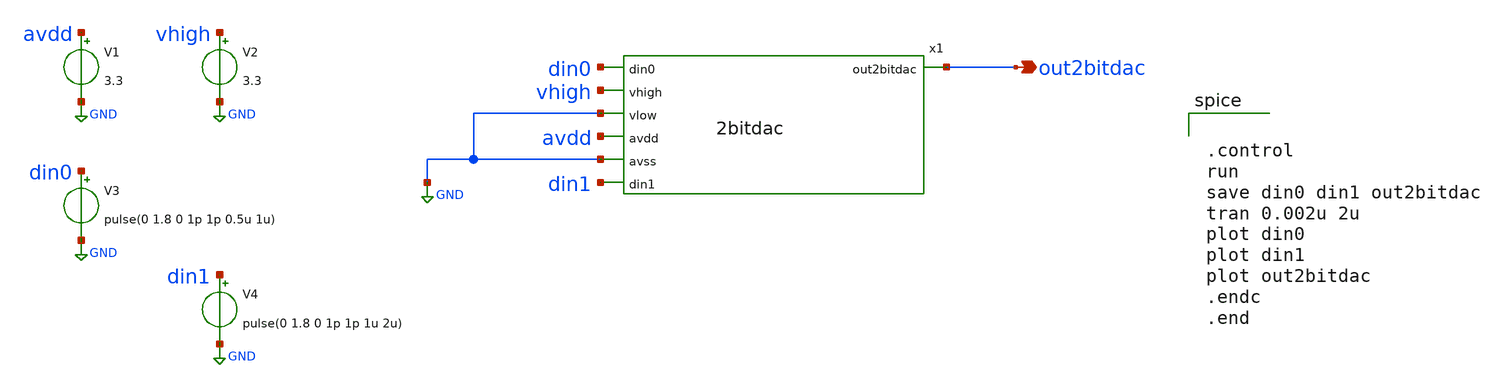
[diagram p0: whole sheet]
** sch_path: xschem/tb_2bitdac.sch
**.subckt tb_2bitdac out2bitdac
*.opin out2bitdac
x1 out2bitdac din0 vhigh GND avdd GND din1 2bitdac
V1 avdd GND 3.3
V2 vhigh GND 3.3
V3 din0 GND pulse(0 1.8 0 1p 1p 0.5u 1u)
V4 din1 GND pulse(0 1.8 0 1p 1p 1u 2u)
**** begin user architecture code

** opencircuitdesign pdks install
.lib $::SKYWATER_MODELS/sky130.lib.spice tt




.control
run
save din0 din1 out2bitdac
tran 0.002u 2u
plot din0
plot din1
plot out2bitdac
.endc
.end

**** end user architecture code
**.ends

* expanding   symbol:  2bitdac.sym # of pins=7
** sym_path: xschem/2bitdac.sym
** sch_path: xschem/2bitdac.sch
.subckt 2bitdac out2bitdac din0 vhigh vlow avdd avss din1
*.ipin din0
*.ipin vhigh
*.ipin vlow
*.ipin avdd
*.ipin avss
*.ipin din1
*.opin out2bitdac
x1 x1_out net1 net2 avss avdd din0 switch
x2 x2_out net3 vlow avss avdd din0 switch
x3 out2bitdac x1_out x2_out avss avdd din1 switch
XR6 net1 vhigh avss sky130_fd_pr__res_high_po_0p35 L=3 mult=1 m=1
XR1 net2 net1 avss sky130_fd_pr__res_high_po_0p35 L=3 mult=1 m=1
XR2 net3 net2 avss sky130_fd_pr__res_high_po_0p35 L=3 mult=1 m=1
XR3 vlow net3 avss sky130_fd_pr__res_high_po_0p35 L=3 mult=1 m=1
.ends


* expanding   symbol:  switch.sym # of pins=6
** sym_path: xschem/switch.sym
** sch_path: xschem/switch.sch
.subckt switch outsw in1 in2 avss avdd din
*.ipin avss
*.ipin avdd
*.ipin din
*.ipin in1
*.ipin in2
*.opin outsw
XM10 dinbar din avdd avdd sky130_fd_pr__pfet_g5v0d10v5 L=0.5 W=1 nf=1 ad='int((1 + 1)/2) * 1 / 1 * 0.29'
+ as='int((1 + 2)/2) * 1 / 1 * 0.29' pd='2*int((1 + 1)/2) * (1 / 1 + 0.29)' ps='2*int((1 + 2)/2) * (1 / 1 + 0.29)'
+ nrd='0.29 / 1 ' nrs='0.29 / 1 ' sa=0 sb=0 sd=0 mult=1 m=1
XM2 dinbar din avss avss sky130_fd_pr__nfet_g5v0d10v5 L=0.5 W=1 nf=1 ad='int((1 + 1)/2) * 1 / 1 * 0.29'
+ as='int((1 + 2)/2) * 1 / 1 * 0.29' pd='2*int((1 + 1)/2) * (1 / 1 + 0.29)' ps='2*int((1 + 2)/2) * (1 / 1 + 0.29)'
+ nrd='0.29 / 1 ' nrs='0.29 / 1 ' sa=0 sb=0 sd=0 mult=1 m=1
XM1 wc dinbar avdd avdd sky130_fd_pr__pfet_g5v0d10v5 L=0.5 W=1 nf=1 ad='int((1 + 1)/2) * 1 / 1 * 0.29'
+ as='int((1 + 2)/2) * 1 / 1 * 0.29' pd='2*int((1 + 1)/2) * (1 / 1 + 0.29)' ps='2*int((1 + 2)/2) * (1 / 1 + 0.29)'
+ nrd='0.29 / 1 ' nrs='0.29 / 1 ' sa=0 sb=0 sd=0 mult=1 m=1
XM3 wc dinbar avss avss sky130_fd_pr__nfet_g5v0d10v5 L=0.5 W=1 nf=1 ad='int((1 + 1)/2) * 1 / 1 * 0.29'
+ as='int((1 + 2)/2) * 1 / 1 * 0.29' pd='2*int((1 + 1)/2) * (1 / 1 + 0.29)' ps='2*int((1 + 2)/2) * (1 / 1 + 0.29)'
+ nrd='0.29 / 1 ' nrs='0.29 / 1 ' sa=0 sb=0 sd=0 mult=1 m=1
XM5 outsw dinbar in2 avss sky130_fd_pr__nfet_g5v0d10v5 L=0.5 W=1 nf=1 ad='int((1 + 1)/2) * 1 / 1 * 0.29'
+ as='int((1 + 2)/2) * 1 / 1 * 0.29' pd='2*int((1 + 1)/2) * (1 / 1 + 0.29)' ps='2*int((1 + 2)/2) * (1 / 1 + 0.29)'
+ nrd='0.29 / 1 ' nrs='0.29 / 1 ' sa=0 sb=0 sd=0 mult=1 m=1
XM4 outsw dinbar in1 avdd sky130_fd_pr__pfet_g5v0d10v5 L=0.5 W=1 nf=1 ad='int((1 + 1)/2) * 1 / 1 * 0.29'
+ as='int((1 + 2)/2) * 1 / 1 * 0.29' pd='2*int((1 + 1)/2) * (1 / 1 + 0.29)' ps='2*int((1 + 2)/2) * (1 / 1 + 0.29)'
+ nrd='0.29 / 1 ' nrs='0.29 / 1 ' sa=0 sb=0 sd=0 mult=1 m=1
XM11 in2 wc outsw avdd sky130_fd_pr__pfet_g5v0d10v5 L=0.5 W=1 nf=1 ad='int((1 + 1)/2) * 1 / 1 * 0.29'
+ as='int((1 + 2)/2) * 1 / 1 * 0.29' pd='2*int((1 + 1)/2) * (1 / 1 + 0.29)' ps='2*int((1 + 2)/2) * (1 / 1 + 0.29)'
+ nrd='0.29 / 1 ' nrs='0.29 / 1 ' sa=0 sb=0 sd=0 mult=1 m=1
XM12 in1 wc outsw avss sky130_fd_pr__nfet_g5v0d10v5 L=0.5 W=1 nf=1 ad='int((1 + 1)/2) * 1 / 1 * 0.29'
+ as='int((1 + 2)/2) * 1 / 1 * 0.29' pd='2*int((1 + 1)/2) * (1 / 1 + 0.29)' ps='2*int((1 + 2)/2) * (1 / 1 + 0.29)'
+ nrd='0.29 / 1 ' nrs='0.29 / 1 ' sa=0 sb=0 sd=0 mult=1 m=1
.ends

.GLOBAL GND
.end
